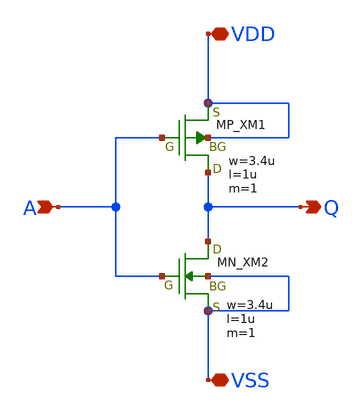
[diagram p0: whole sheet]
** sch_path: inverter/inverter_Takata_Ibuki.sch
**.subckt inverter_Takata_Ibuki A Q VDD VSS
*.ipin A
*.opin Q
*.iopin VDD
*.iopin VSS
XXM1 Q A VDD VDD PMOS w=3.4u l=1u nrd=0 nrs=0 m=1
XXM2 Q A VSS VSS NMOS w=3.4u l=1u nrd=0 nrs=0 m=1
**.ends
.end
